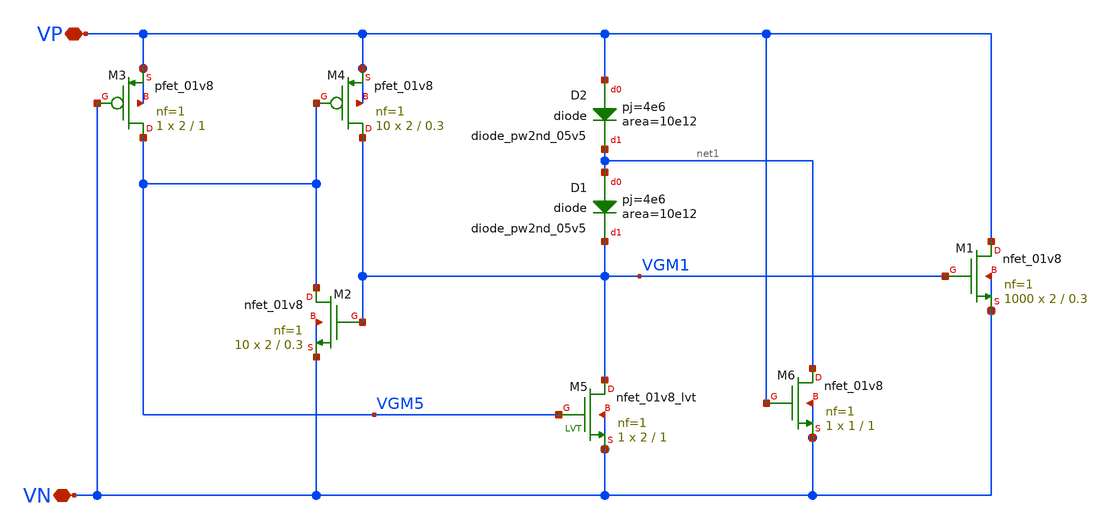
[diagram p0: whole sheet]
** sch_path: xschem/esd/esd_clamp.sch
**.subckt esd_clamp VP VN
*.iopin VP
*.iopin VN
XD1 net1 VGM1 sky130_fd_pr__diode_pw2nd_05v5 area=10e12 pj=4e6
XM3 VGM5 VN VP VP sky130_fd_pr__pfet_01v8 L=1 W=2 nf=1 ad='int((nf+1)/2) * W/nf * 0.29' as='int((nf+2)/2) * W/nf * 0.29'
+ pd='2*int((nf+1)/2) * (W/nf + 0.29)' ps='2*int((nf+2)/2) * (W/nf + 0.29)' nrd='0.29 / W' nrs='0.29 / W'
+ sa=0 sb=0 sd=0 mult=1 m=1
XM4 VGM1 VGM5 VP VP sky130_fd_pr__pfet_01v8 L=0.3 W=2 nf=1 ad='int((nf+1)/2) * W/nf * 0.29' as='int((nf+2)/2) * W/nf * 0.29'
+ pd='2*int((nf+1)/2) * (W/nf + 0.29)' ps='2*int((nf+2)/2) * (W/nf + 0.29)' nrd='0.29 / W' nrs='0.29 / W'
+ sa=0 sb=0 sd=0 mult=10 m=10
XM5 VGM1 VGM5 VN VN sky130_fd_pr__nfet_01v8_lvt L=1 W=2 nf=1 ad='int((nf+1)/2) * W/nf * 0.29' as='int((nf+2)/2) * W/nf * 0.29'
+ pd='2*int((nf+1)/2) * (W/nf + 0.29)' ps='2*int((nf+2)/2) * (W/nf + 0.29)' nrd='0.29 / W' nrs='0.29 / W'
+ sa=0 sb=0 sd=0 mult=1 m=1
XD2 VP net1 sky130_fd_pr__diode_pw2nd_05v5 area=10e12 pj=4e6
XM1 VP VGM1 VN VN sky130_fd_pr__nfet_01v8 L=0.3 W=2 nf=1 ad='int((nf+1)/2) * W/nf * 0.29' as='int((nf+2)/2) * W/nf * 0.29'
+ pd='2*int((nf+1)/2) * (W/nf + 0.29)' ps='2*int((nf+2)/2) * (W/nf + 0.29)' nrd='0.29 / W' nrs='0.29 / W'
+ sa=0 sb=0 sd=0 mult=1000 m=1000
XM6 net1 VP VN VN sky130_fd_pr__nfet_01v8 L=1 W=1 nf=1 ad='int((nf+1)/2) * W/nf * 0.29' as='int((nf+2)/2) * W/nf * 0.29'
+ pd='2*int((nf+1)/2) * (W/nf + 0.29)' ps='2*int((nf+2)/2) * (W/nf + 0.29)' nrd='0.29 / W' nrs='0.29 / W'
+ sa=0 sb=0 sd=0 mult=1 m=1
XM2 VGM5 VGM1 VN VN sky130_fd_pr__nfet_01v8 L=0.3 W=2 nf=1 ad='int((nf+1)/2) * W/nf * 0.29' as='int((nf+2)/2) * W/nf * 0.29'
+ pd='2*int((nf+1)/2) * (W/nf + 0.29)' ps='2*int((nf+2)/2) * (W/nf + 0.29)' nrd='0.29 / W' nrs='0.29 / W'
+ sa=0 sb=0 sd=0 mult=10 m=10
**.ends
.end
